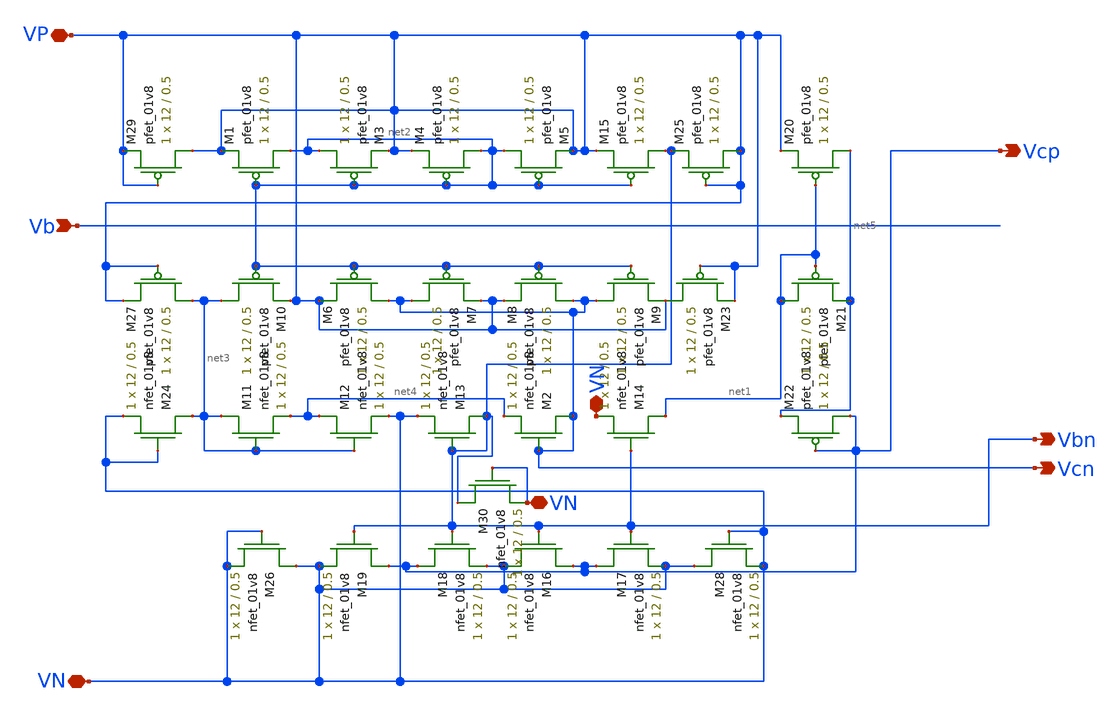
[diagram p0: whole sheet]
** sch_path: MiniProject3-Cascode/XSCHEM/Schematics/VoltageGenerator.sch
**.subckt VoltageGenerator VP VN Vcn Vcp Vbn Vb VN VN
*.iopin VP
*.iopin VN
*.opin Vcn
*.opin Vcp
*.opin Vbn
*.ipin Vb
*.iopin VN
*.iopin VN
XM1 net2 net2 VP VP sky130_fd_pr__pfet_01v8 L=0.5 W=12 nf=1 ad='int((nf+1)/2) * W/nf * 0.29' as='int((nf+2)/2) * W/nf * 0.29'
+ pd='2*int((nf+1)/2) * (W/nf + 0.29)' ps='2*int((nf+2)/2) * (W/nf + 0.29)' nrd='0.29 / W' nrs='0.29 / W'
+ sa=0 sb=0 sd=0 mult=1 m=1
XM2 Vcn Vcn net4 VN sky130_fd_pr__nfet_01v8 L=0.5 W=12 nf=1 ad='int((nf+1)/2) * W/nf * 0.29' as='int((nf+2)/2) * W/nf * 0.29'
+ pd='2*int((nf+1)/2) * (W/nf + 0.29)' ps='2*int((nf+2)/2) * (W/nf + 0.29)' nrd='0.29 / W' nrs='0.29 / W'
+ sa=0 sb=0 sd=0 mult=1 m=1
XM3 net2 net2 VP VP sky130_fd_pr__pfet_01v8 L=0.5 W=12 nf=1 ad='int((nf+1)/2) * W/nf * 0.29' as='int((nf+2)/2) * W/nf * 0.29'
+ pd='2*int((nf+1)/2) * (W/nf + 0.29)' ps='2*int((nf+2)/2) * (W/nf + 0.29)' nrd='0.29 / W' nrs='0.29 / W'
+ sa=0 sb=0 sd=0 mult=1 m=1
XM4 net2 net2 VP VP sky130_fd_pr__pfet_01v8 L=0.5 W=12 nf=1 ad='int((nf+1)/2) * W/nf * 0.29' as='int((nf+2)/2) * W/nf * 0.29'
+ pd='2*int((nf+1)/2) * (W/nf + 0.29)' ps='2*int((nf+2)/2) * (W/nf + 0.29)' nrd='0.29 / W' nrs='0.29 / W'
+ sa=0 sb=0 sd=0 mult=1 m=1
XM5 net2 net2 VP VP sky130_fd_pr__pfet_01v8 L=0.5 W=12 nf=1 ad='int((nf+1)/2) * W/nf * 0.29' as='int((nf+2)/2) * W/nf * 0.29'
+ pd='2*int((nf+1)/2) * (W/nf + 0.29)' ps='2*int((nf+2)/2) * (W/nf + 0.29)' nrd='0.29 / W' nrs='0.29 / W'
+ sa=0 sb=0 sd=0 mult=1 m=1
XM6 Vcn net2 VP VP sky130_fd_pr__pfet_01v8 L=0.5 W=12 nf=1 ad='int((nf+1)/2) * W/nf * 0.29' as='int((nf+2)/2) * W/nf * 0.29'
+ pd='2*int((nf+1)/2) * (W/nf + 0.29)' ps='2*int((nf+2)/2) * (W/nf + 0.29)' nrd='0.29 / W' nrs='0.29 / W'
+ sa=0 sb=0 sd=0 mult=1 m=1
XM7 Vcn net2 VP VP sky130_fd_pr__pfet_01v8 L=0.5 W=12 nf=1 ad='int((nf+1)/2) * W/nf * 0.29' as='int((nf+2)/2) * W/nf * 0.29'
+ pd='2*int((nf+1)/2) * (W/nf + 0.29)' ps='2*int((nf+2)/2) * (W/nf + 0.29)' nrd='0.29 / W' nrs='0.29 / W'
+ sa=0 sb=0 sd=0 mult=1 m=1
XM8 Vcn net2 VP VP sky130_fd_pr__pfet_01v8 L=0.5 W=12 nf=1 ad='int((nf+1)/2) * W/nf * 0.29' as='int((nf+2)/2) * W/nf * 0.29'
+ pd='2*int((nf+1)/2) * (W/nf + 0.29)' ps='2*int((nf+2)/2) * (W/nf + 0.29)' nrd='0.29 / W' nrs='0.29 / W'
+ sa=0 sb=0 sd=0 mult=1 m=1
XM9 Vcn net2 VP VP sky130_fd_pr__pfet_01v8 L=0.5 W=12 nf=1 ad='int((nf+1)/2) * W/nf * 0.29' as='int((nf+2)/2) * W/nf * 0.29'
+ pd='2*int((nf+1)/2) * (W/nf + 0.29)' ps='2*int((nf+2)/2) * (W/nf + 0.29)' nrd='0.29 / W' nrs='0.29 / W'
+ sa=0 sb=0 sd=0 mult=1 m=1
XM10 net3 net2 VP VP sky130_fd_pr__pfet_01v8 L=0.5 W=12 nf=1 ad='int((nf+1)/2) * W/nf * 0.29' as='int((nf+2)/2) * W/nf * 0.29'
+ pd='2*int((nf+1)/2) * (W/nf + 0.29)' ps='2*int((nf+2)/2) * (W/nf + 0.29)' nrd='0.29 / W' nrs='0.29 / W'
+ sa=0 sb=0 sd=0 mult=1 m=1
XM11 net3 net3 net4 VN sky130_fd_pr__nfet_01v8 L=0.5 W=12 nf=1 ad='int((nf+1)/2) * W/nf * 0.29' as='int((nf+2)/2) * W/nf * 0.29'
+ pd='2*int((nf+1)/2) * (W/nf + 0.29)' ps='2*int((nf+2)/2) * (W/nf + 0.29)' nrd='0.29 / W' nrs='0.29 / W'
+ sa=0 sb=0 sd=0 mult=1 m=1
XM12 net4 net3 VN VN sky130_fd_pr__nfet_01v8 L=0.5 W=12 nf=1 ad='int((nf+1)/2) * W/nf * 0.29' as='int((nf+2)/2) * W/nf * 0.29'
+ pd='2*int((nf+1)/2) * (W/nf + 0.29)' ps='2*int((nf+2)/2) * (W/nf + 0.29)' nrd='0.29 / W' nrs='0.29 / W'
+ sa=0 sb=0 sd=0 mult=1 m=1
XM13 Vbn Vbn VN VN sky130_fd_pr__nfet_01v8 L=0.5 W=12 nf=1 ad='int((nf+1)/2) * W/nf * 0.29' as='int((nf+2)/2) * W/nf * 0.29'
+ pd='2*int((nf+1)/2) * (W/nf + 0.29)' ps='2*int((nf+2)/2) * (W/nf + 0.29)' nrd='0.29 / W' nrs='0.29 / W'
+ sa=0 sb=0 sd=0 mult=1 m=1
XM14 net1 Vbn VN VN sky130_fd_pr__nfet_01v8 L=0.5 W=12 nf=1 ad='int((nf+1)/2) * W/nf * 0.29' as='int((nf+2)/2) * W/nf * 0.29'
+ pd='2*int((nf+1)/2) * (W/nf + 0.29)' ps='2*int((nf+2)/2) * (W/nf + 0.29)' nrd='0.29 / W' nrs='0.29 / W'
+ sa=0 sb=0 sd=0 mult=1 m=1
XM15 Vbn net2 VP VP sky130_fd_pr__pfet_01v8 L=0.5 W=12 nf=1 ad='int((nf+1)/2) * W/nf * 0.29' as='int((nf+2)/2) * W/nf * 0.29'
+ pd='2*int((nf+1)/2) * (W/nf + 0.29)' ps='2*int((nf+2)/2) * (W/nf + 0.29)' nrd='0.29 / W' nrs='0.29 / W'
+ sa=0 sb=0 sd=0 mult=1 m=1
XM16 Vcp Vbn VN VN sky130_fd_pr__nfet_01v8 L=0.5 W=12 nf=1 ad='int((nf+1)/2) * W/nf * 0.29' as='int((nf+2)/2) * W/nf * 0.29'
+ pd='2*int((nf+1)/2) * (W/nf + 0.29)' ps='2*int((nf+2)/2) * (W/nf + 0.29)' nrd='0.29 / W' nrs='0.29 / W'
+ sa=0 sb=0 sd=0 mult=1 m=1
XM17 Vcp Vbn VN VN sky130_fd_pr__nfet_01v8 L=0.5 W=12 nf=1 ad='int((nf+1)/2) * W/nf * 0.29' as='int((nf+2)/2) * W/nf * 0.29'
+ pd='2*int((nf+1)/2) * (W/nf + 0.29)' ps='2*int((nf+2)/2) * (W/nf + 0.29)' nrd='0.29 / W' nrs='0.29 / W'
+ sa=0 sb=0 sd=0 mult=1 m=1
XM18 Vcp Vbn VN VN sky130_fd_pr__nfet_01v8 L=0.5 W=12 nf=1 ad='int((nf+1)/2) * W/nf * 0.29' as='int((nf+2)/2) * W/nf * 0.29'
+ pd='2*int((nf+1)/2) * (W/nf + 0.29)' ps='2*int((nf+2)/2) * (W/nf + 0.29)' nrd='0.29 / W' nrs='0.29 / W'
+ sa=0 sb=0 sd=0 mult=1 m=1
XM19 Vcp Vbn VN VN sky130_fd_pr__nfet_01v8 L=0.5 W=12 nf=1 ad='int((nf+1)/2) * W/nf * 0.29' as='int((nf+2)/2) * W/nf * 0.29'
+ pd='2*int((nf+1)/2) * (W/nf + 0.29)' ps='2*int((nf+2)/2) * (W/nf + 0.29)' nrd='0.29 / W' nrs='0.29 / W'
+ sa=0 sb=0 sd=0 mult=1 m=1
XM20 net5 net1 VP VP sky130_fd_pr__pfet_01v8 L=0.5 W=12 nf=1 ad='int((nf+1)/2) * W/nf * 0.29' as='int((nf+2)/2) * W/nf * 0.29'
+ pd='2*int((nf+1)/2) * (W/nf + 0.29)' ps='2*int((nf+2)/2) * (W/nf + 0.29)' nrd='0.29 / W' nrs='0.29 / W'
+ sa=0 sb=0 sd=0 mult=1 m=1
XM21 net1 net1 net5 VP sky130_fd_pr__pfet_01v8 L=0.5 W=12 nf=1 ad='int((nf+1)/2) * W/nf * 0.29' as='int((nf+2)/2) * W/nf * 0.29'
+ pd='2*int((nf+1)/2) * (W/nf + 0.29)' ps='2*int((nf+2)/2) * (W/nf + 0.29)' nrd='0.29 / W' nrs='0.29 / W'
+ sa=0 sb=0 sd=0 mult=1 m=1
XM22 Vcp Vcp net5 VP sky130_fd_pr__pfet_01v8 L=0.5 W=12 nf=1 ad='int((nf+1)/2) * W/nf * 0.29' as='int((nf+2)/2) * W/nf * 0.29'
+ pd='2*int((nf+1)/2) * (W/nf + 0.29)' ps='2*int((nf+2)/2) * (W/nf + 0.29)' nrd='0.29 / W' nrs='0.29 / W'
+ sa=0 sb=0 sd=0 mult=1 m=1
XM23 VP VP VP VP sky130_fd_pr__pfet_01v8 L=0.5 W=12 nf=1 ad='int((nf+1)/2) * W/nf * 0.29' as='int((nf+2)/2) * W/nf * 0.29'
+ pd='2*int((nf+1)/2) * (W/nf + 0.29)' ps='2*int((nf+2)/2) * (W/nf + 0.29)' nrd='0.29 / W' nrs='0.29 / W'
+ sa=0 sb=0 sd=0 mult=1 m=1
XM25 VP VP Vbn VP sky130_fd_pr__pfet_01v8 L=0.5 W=12 nf=1 ad='int((nf+1)/2) * W/nf * 0.29' as='int((nf+2)/2) * W/nf * 0.29'
+ pd='2*int((nf+1)/2) * (W/nf + 0.29)' ps='2*int((nf+2)/2) * (W/nf + 0.29)' nrd='0.29 / W' nrs='0.29 / W'
+ sa=0 sb=0 sd=0 mult=1 m=1
XM30 Vbn VN VN VN sky130_fd_pr__nfet_01v8 L=0.5 W=12 nf=1 ad='int((nf+1)/2) * W/nf * 0.29' as='int((nf+2)/2) * W/nf * 0.29'
+ pd='2*int((nf+1)/2) * (W/nf + 0.29)' ps='2*int((nf+2)/2) * (W/nf + 0.29)' nrd='0.29 / W' nrs='0.29 / W'
+ sa=0 sb=0 sd=0 mult=1 m=1
XM26 VN VN VN VN sky130_fd_pr__nfet_01v8 L=0.5 W=12 nf=1 ad='int((nf+1)/2) * W/nf * 0.29' as='int((nf+2)/2) * W/nf * 0.29'
+ pd='2*int((nf+1)/2) * (W/nf + 0.29)' ps='2*int((nf+2)/2) * (W/nf + 0.29)' nrd='0.29 / W' nrs='0.29 / W'
+ sa=0 sb=0 sd=0 mult=1 m=1
XM28 VN VN VN VN sky130_fd_pr__nfet_01v8 L=0.5 W=12 nf=1 ad='int((nf+1)/2) * W/nf * 0.29' as='int((nf+2)/2) * W/nf * 0.29'
+ pd='2*int((nf+1)/2) * (W/nf + 0.29)' ps='2*int((nf+2)/2) * (W/nf + 0.29)' nrd='0.29 / W' nrs='0.29 / W'
+ sa=0 sb=0 sd=0 mult=1 m=1
XM24 net3 VN VN VN sky130_fd_pr__nfet_01v8 L=0.5 W=12 nf=1 ad='int((nf+1)/2) * W/nf * 0.29' as='int((nf+2)/2) * W/nf * 0.29'
+ pd='2*int((nf+1)/2) * (W/nf + 0.29)' ps='2*int((nf+2)/2) * (W/nf + 0.29)' nrd='0.29 / W' nrs='0.29 / W'
+ sa=0 sb=0 sd=0 mult=1 m=1
XM27 net3 VP VP VP sky130_fd_pr__pfet_01v8 L=0.5 W=12 nf=1 ad='int((nf+1)/2) * W/nf * 0.29' as='int((nf+2)/2) * W/nf * 0.29'
+ pd='2*int((nf+1)/2) * (W/nf + 0.29)' ps='2*int((nf+2)/2) * (W/nf + 0.29)' nrd='0.29 / W' nrs='0.29 / W'
+ sa=0 sb=0 sd=0 mult=1 m=1
XM29 VP VP VP VP sky130_fd_pr__pfet_01v8 L=0.5 W=12 nf=1 ad='int((nf+1)/2) * W/nf * 0.29' as='int((nf+2)/2) * W/nf * 0.29'
+ pd='2*int((nf+1)/2) * (W/nf + 0.29)' ps='2*int((nf+2)/2) * (W/nf + 0.29)' nrd='0.29 / W' nrs='0.29 / W'
+ sa=0 sb=0 sd=0 mult=1 m=1
**.ends
.end
